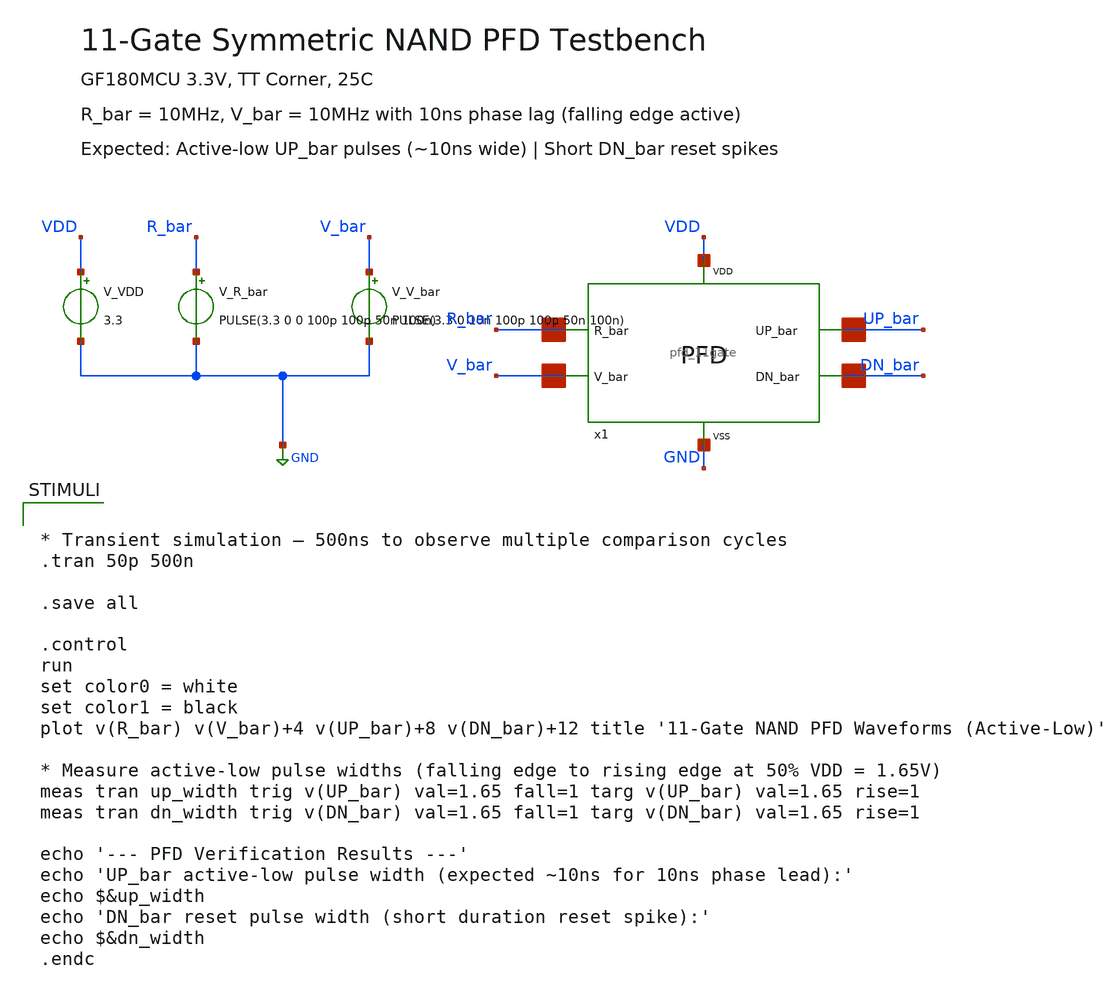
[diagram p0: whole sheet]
** sch_path: designs/libs/tb_analog/tb_pfd/tb_pfd_11gate.sch
**.subckt tb_pfd_11gate
V_R_bar R_bar GND PULSE(3.3 0 0 100p 100p 50n 100n)
V_V_bar V_bar GND PULSE(3.3 0 10n 100p 100p 50n 100n)
V_VDD VDD GND 3.3
x1 R_bar V_bar UP_bar DN_bar VDD GND pfd_11gate
**** begin user architecture code


* Transient simulation — 500ns to observe multiple comparison cycles
.tran 50p 500n

.save all

.control
run
set color0 = white
set color1 = black
plot v(R_bar) v(V_bar)+4 v(UP_bar)+8 v(DN_bar)+12 title '11-Gate NAND PFD Waveforms (Active-Low)'

* Measure active-low pulse widths (falling edge to rising edge at 50% VDD = 1.65V)
meas tran up_width trig v(UP_bar) val=1.65 fall=1 targ v(UP_bar) val=1.65 rise=1
meas tran dn_width trig v(DN_bar) val=1.65 fall=1 targ v(DN_bar) val=1.65 rise=1

echo '--- PFD Verification Results ---'
echo 'UP_bar active-low pulse width (expected ~10ns for 10ns phase lead):'
echo $&up_width
echo 'DN_bar reset pulse width (short duration reset spike):'
echo $&dn_width
.endc



.include /foss/pdks/ciel/gf180mcu/versions/7b70722e33c03fcb5dabcf4d479fb0822d9251c9/gf180mcuD/libs.ref/gf180mcu_fd_sc_mcu7t5v0/spice/gf180mcu_fd_sc_mcu7t5v0.spice
.include $::180MCU_MODELS/design.ngspice
.lib $::180MCU_MODELS/sm141064.ngspice typical

**** end user architecture code
**.ends
.GLOBAL GND
.end
